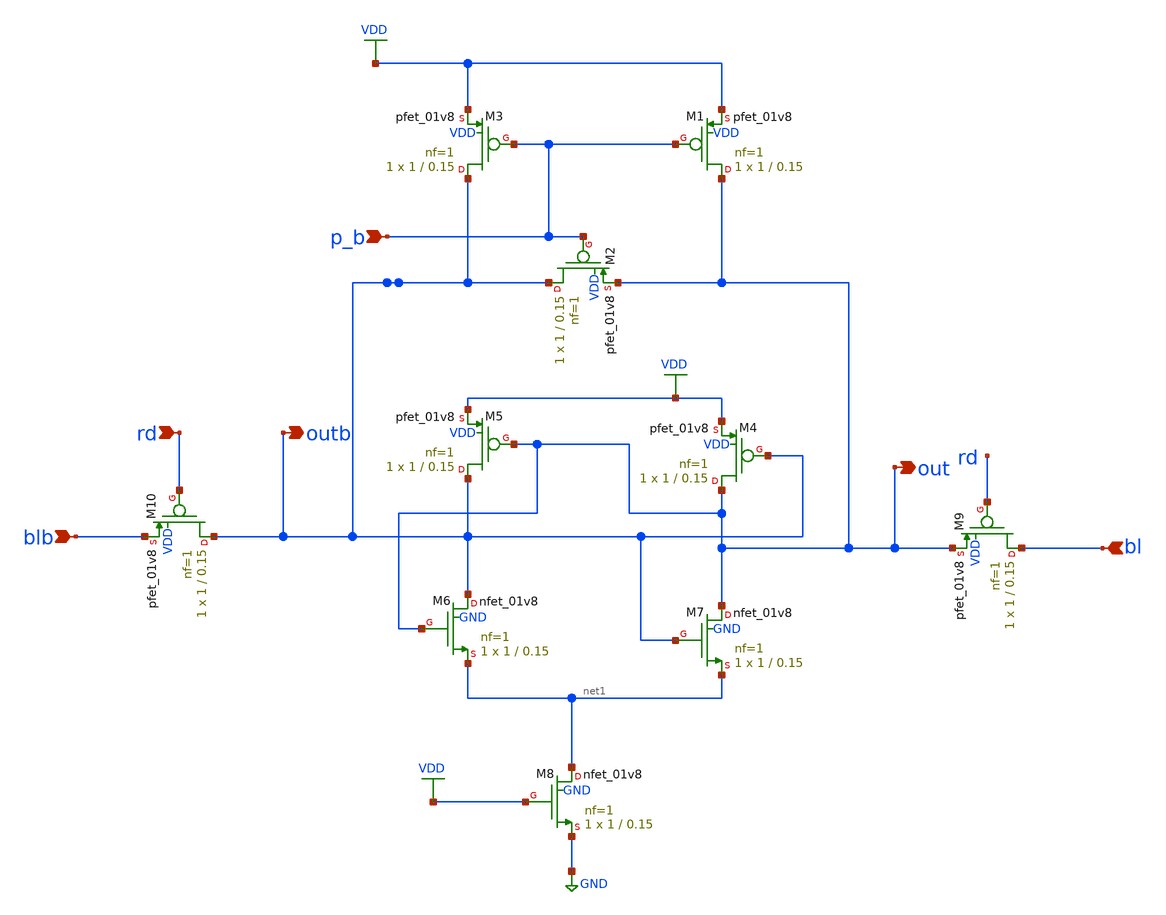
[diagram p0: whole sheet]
** sch_path: gates/Memory/Sense amplifier.sch
**.subckt Sense amplifier p_b rd blb bl out outb
*.ipin p_b
*.ipin rd
*.ipin blb
*.ipin bl
*.opin out
*.opin outb
XM1 out p_b VDD VDD sky130_fd_pr__pfet_01v8 L=0.15 W=1 nf=1 ad='int((nf+1)/2) * W/nf * 0.29' as='int((nf+2)/2) * W/nf * 0.29'
+ pd='2*int((nf+1)/2) * (W/nf + 0.29)' ps='2*int((nf+2)/2) * (W/nf + 0.29)' nrd='0.29 / W' nrs='0.29 / W'
+ sa=0 sb=0 sd=0 mult=1 m=1
XM2 outb p_b out VDD sky130_fd_pr__pfet_01v8 L=0.15 W=1 nf=1 ad='int((nf+1)/2) * W/nf * 0.29' as='int((nf+2)/2) * W/nf * 0.29'
+ pd='2*int((nf+1)/2) * (W/nf + 0.29)' ps='2*int((nf+2)/2) * (W/nf + 0.29)' nrd='0.29 / W' nrs='0.29 / W'
+ sa=0 sb=0 sd=0 mult=1 m=1
XM3 outb p_b VDD VDD sky130_fd_pr__pfet_01v8 L=0.15 W=1 nf=1 ad='int((nf+1)/2) * W/nf * 0.29' as='int((nf+2)/2) * W/nf * 0.29'
+ pd='2*int((nf+1)/2) * (W/nf + 0.29)' ps='2*int((nf+2)/2) * (W/nf + 0.29)' nrd='0.29 / W' nrs='0.29 / W'
+ sa=0 sb=0 sd=0 mult=1 m=1
XM4 out outb VDD VDD sky130_fd_pr__pfet_01v8 L=0.15 W=1 nf=1 ad='int((nf+1)/2) * W/nf * 0.29' as='int((nf+2)/2) * W/nf * 0.29'
+ pd='2*int((nf+1)/2) * (W/nf + 0.29)' ps='2*int((nf+2)/2) * (W/nf + 0.29)' nrd='0.29 / W' nrs='0.29 / W'
+ sa=0 sb=0 sd=0 mult=1 m=1
XM5 outb out VDD VDD sky130_fd_pr__pfet_01v8 L=0.15 W=1 nf=1 ad='int((nf+1)/2) * W/nf * 0.29' as='int((nf+2)/2) * W/nf * 0.29'
+ pd='2*int((nf+1)/2) * (W/nf + 0.29)' ps='2*int((nf+2)/2) * (W/nf + 0.29)' nrd='0.29 / W' nrs='0.29 / W'
+ sa=0 sb=0 sd=0 mult=1 m=1
XM6 outb out net1 GND sky130_fd_pr__nfet_01v8 L=0.15 W=1 nf=1 ad='int((nf+1)/2) * W/nf * 0.29' as='int((nf+2)/2) * W/nf * 0.29'
+ pd='2*int((nf+1)/2) * (W/nf + 0.29)' ps='2*int((nf+2)/2) * (W/nf + 0.29)' nrd='0.29 / W' nrs='0.29 / W'
+ sa=0 sb=0 sd=0 mult=1 m=1
XM7 out outb net1 GND sky130_fd_pr__nfet_01v8 L=0.15 W=1 nf=1 ad='int((nf+1)/2) * W/nf * 0.29' as='int((nf+2)/2) * W/nf * 0.29'
+ pd='2*int((nf+1)/2) * (W/nf + 0.29)' ps='2*int((nf+2)/2) * (W/nf + 0.29)' nrd='0.29 / W' nrs='0.29 / W'
+ sa=0 sb=0 sd=0 mult=1 m=1
XM8 net1 VDD GND GND sky130_fd_pr__nfet_01v8 L=0.15 W=1 nf=1 ad='int((nf+1)/2) * W/nf * 0.29' as='int((nf+2)/2) * W/nf * 0.29'
+ pd='2*int((nf+1)/2) * (W/nf + 0.29)' ps='2*int((nf+2)/2) * (W/nf + 0.29)' nrd='0.29 / W' nrs='0.29 / W'
+ sa=0 sb=0 sd=0 mult=1 m=1
XM9 bl rd out VDD sky130_fd_pr__pfet_01v8 L=0.15 W=1 nf=1 ad='int((nf+1)/2) * W/nf * 0.29' as='int((nf+2)/2) * W/nf * 0.29'
+ pd='2*int((nf+1)/2) * (W/nf + 0.29)' ps='2*int((nf+2)/2) * (W/nf + 0.29)' nrd='0.29 / W' nrs='0.29 / W'
+ sa=0 sb=0 sd=0 mult=1 m=1
XM10 outb rd blb VDD sky130_fd_pr__pfet_01v8 L=0.15 W=1 nf=1 ad='int((nf+1)/2) * W/nf * 0.29' as='int((nf+2)/2) * W/nf * 0.29'
+ pd='2*int((nf+1)/2) * (W/nf + 0.29)' ps='2*int((nf+2)/2) * (W/nf + 0.29)' nrd='0.29 / W' nrs='0.29 / W'
+ sa=0 sb=0 sd=0 mult=1 m=1
**.ends
.GLOBAL VDD
.GLOBAL GND
.end
